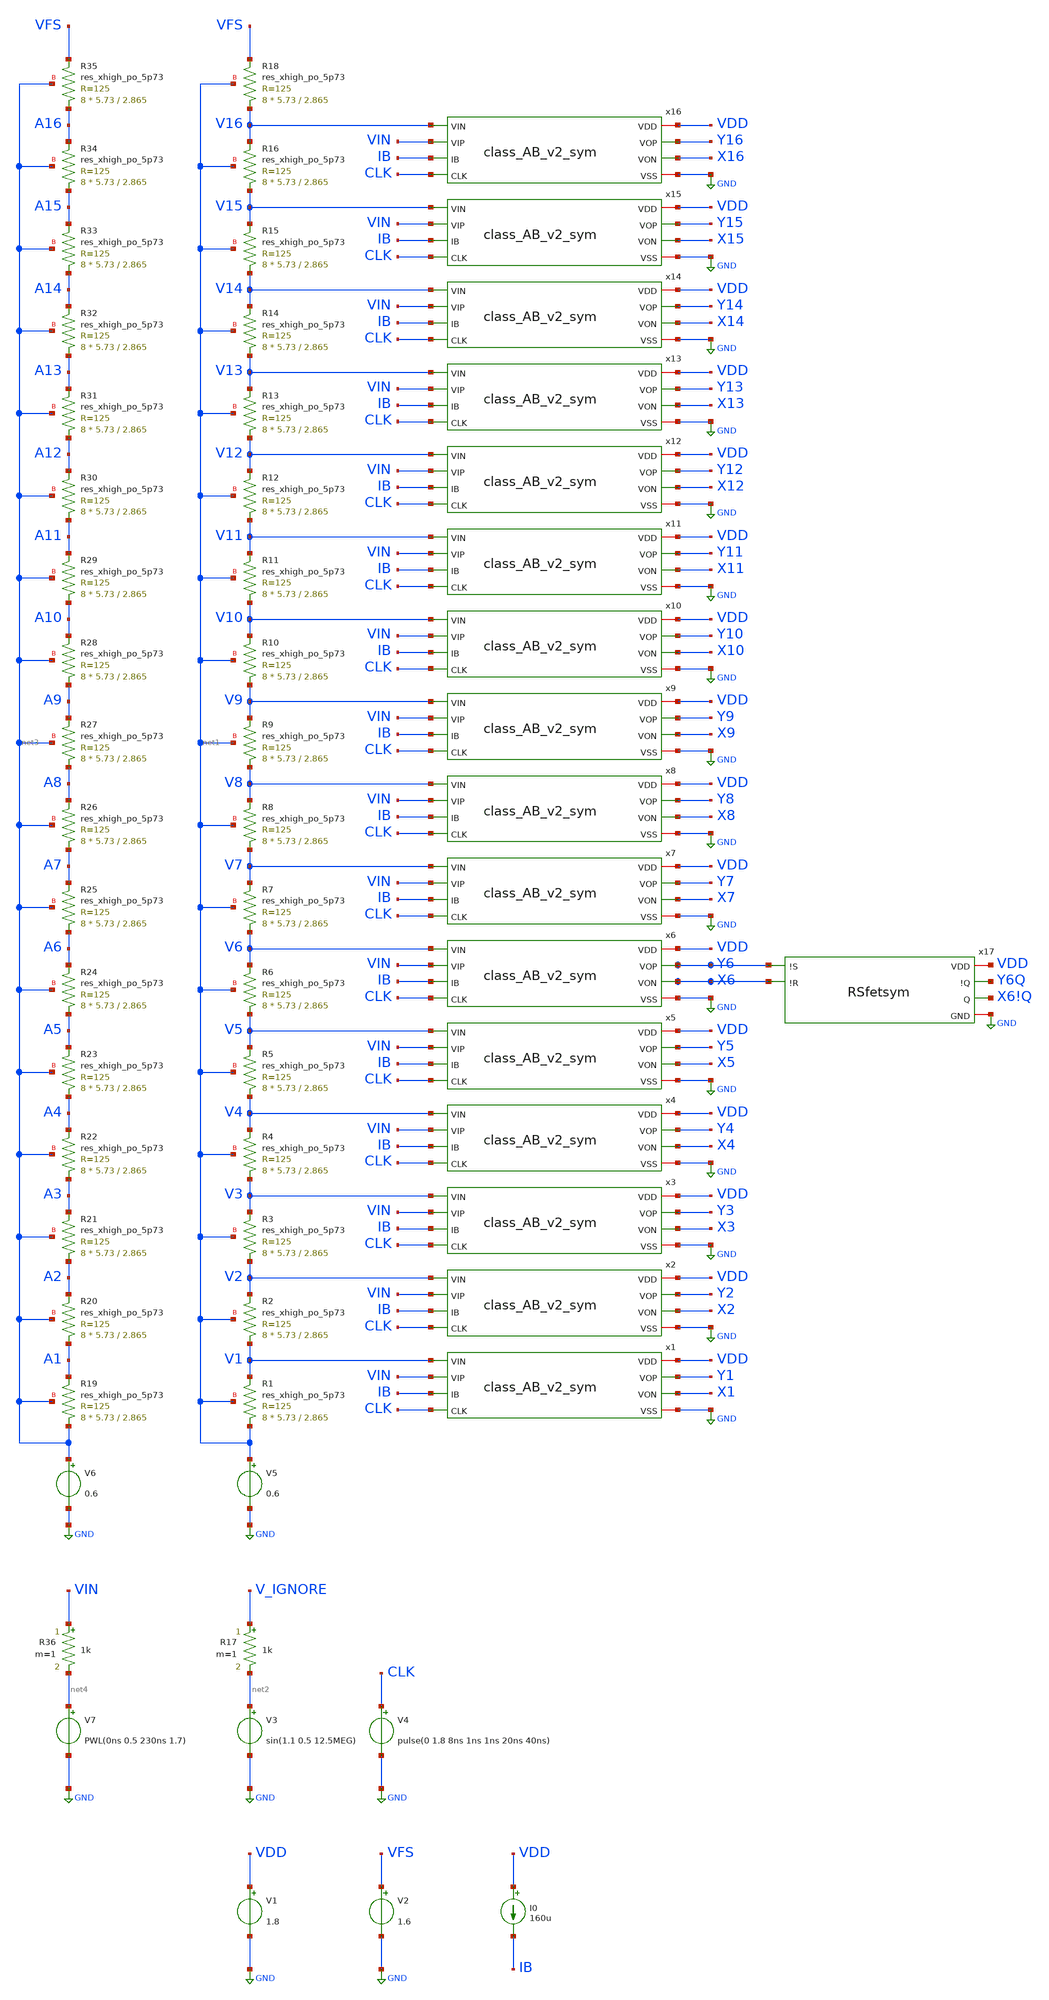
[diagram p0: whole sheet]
** sch_path: testbench/flash_ADC_4b_v2.sch
.lib $::SKYWATER_MODELS/sky130.lib.spice tt
.include $::SKYWATER_STDCELLS/sky130_fd_sc_hd.spice

**.subckt flash_ADC_4b_v2
V3 net2 GND sin(1.1 0.5 12.5MEG)
V4 CLK GND pulse(0 1.8 8ns 1ns 1ns 20ns 40ns)
V1 VDD GND 1.8
V2 VFS GND 1.6
R17 V_IGNORE net2 1k m=1
I0 VDD IB 160u
V5 net1 GND 0.6
XR19 net3 A1 net3 sky130_fd_pr__res_xhigh_po_5p73 L=2.865 mult=8 m=8
V6 net3 GND 0.6
XR20 A1 A2 net3 sky130_fd_pr__res_xhigh_po_5p73 L=2.865 mult=8 m=8
XR21 A2 A3 net3 sky130_fd_pr__res_xhigh_po_5p73 L=2.865 mult=8 m=8
XR22 A3 A4 net3 sky130_fd_pr__res_xhigh_po_5p73 L=2.865 mult=8 m=8
XR23 A4 A5 net3 sky130_fd_pr__res_xhigh_po_5p73 L=2.865 mult=8 m=8
XR24 A5 A6 net3 sky130_fd_pr__res_xhigh_po_5p73 L=2.865 mult=8 m=8
XR25 A6 A7 net3 sky130_fd_pr__res_xhigh_po_5p73 L=2.865 mult=8 m=8
XR26 A7 A8 net3 sky130_fd_pr__res_xhigh_po_5p73 L=2.865 mult=8 m=8
XR27 A8 A9 net3 sky130_fd_pr__res_xhigh_po_5p73 L=2.865 mult=8 m=8
XR28 A9 A10 net3 sky130_fd_pr__res_xhigh_po_5p73 L=2.865 mult=8 m=8
XR29 A10 A11 net3 sky130_fd_pr__res_xhigh_po_5p73 L=2.865 mult=8 m=8
XR30 A11 A12 net3 sky130_fd_pr__res_xhigh_po_5p73 L=2.865 mult=8 m=8
XR31 A12 A13 net3 sky130_fd_pr__res_xhigh_po_5p73 L=2.865 mult=8 m=8
XR32 A13 A14 net3 sky130_fd_pr__res_xhigh_po_5p73 L=2.865 mult=8 m=8
XR33 A14 A15 net3 sky130_fd_pr__res_xhigh_po_5p73 L=2.865 mult=8 m=8
XR34 A15 A16 net3 sky130_fd_pr__res_xhigh_po_5p73 L=2.865 mult=8 m=8
XR35 A16 VFS net3 sky130_fd_pr__res_xhigh_po_5p73 L=2.865 mult=8 m=8
XR1 net1 V1 net1 sky130_fd_pr__res_xhigh_po_5p73 L=2.865 mult=8 m=8
XR2 V1 V2 net1 sky130_fd_pr__res_xhigh_po_5p73 L=2.865 mult=8 m=8
XR3 V2 V3 net1 sky130_fd_pr__res_xhigh_po_5p73 L=2.865 mult=8 m=8
XR4 V3 V4 net1 sky130_fd_pr__res_xhigh_po_5p73 L=2.865 mult=8 m=8
XR5 V4 V5 net1 sky130_fd_pr__res_xhigh_po_5p73 L=2.865 mult=8 m=8
XR6 V5 V6 net1 sky130_fd_pr__res_xhigh_po_5p73 L=2.865 mult=8 m=8
XR7 V6 V7 net1 sky130_fd_pr__res_xhigh_po_5p73 L=2.865 mult=8 m=8
XR8 V7 V8 net1 sky130_fd_pr__res_xhigh_po_5p73 L=2.865 mult=8 m=8
XR9 V8 V9 net1 sky130_fd_pr__res_xhigh_po_5p73 L=2.865 mult=8 m=8
XR10 V9 V10 net1 sky130_fd_pr__res_xhigh_po_5p73 L=2.865 mult=8 m=8
XR11 V10 V11 net1 sky130_fd_pr__res_xhigh_po_5p73 L=2.865 mult=8 m=8
XR12 V11 V12 net1 sky130_fd_pr__res_xhigh_po_5p73 L=2.865 mult=8 m=8
XR13 V12 V13 net1 sky130_fd_pr__res_xhigh_po_5p73 L=2.865 mult=8 m=8
XR14 V13 V14 net1 sky130_fd_pr__res_xhigh_po_5p73 L=2.865 mult=8 m=8
XR15 V14 V15 net1 sky130_fd_pr__res_xhigh_po_5p73 L=2.865 mult=8 m=8
XR16 V15 V16 net1 sky130_fd_pr__res_xhigh_po_5p73 L=2.865 mult=8 m=8
XR18 V16 VFS net1 sky130_fd_pr__res_xhigh_po_5p73 L=2.865 mult=8 m=8
V7 net4 GND PWL(0ns 0.5 230ns 1.7)
R36 VIN net4 1k m=1
x1 VDD Y1 X1 V1 VIN IB CLK GND class_AB_v2_sym
x2 VDD Y2 X2 V2 VIN IB CLK GND class_AB_v2_sym
x3 VDD Y3 X3 V3 VIN IB CLK GND class_AB_v2_sym
x4 VDD Y4 X4 V4 VIN IB CLK GND class_AB_v2_sym
x5 VDD Y5 X5 V5 VIN IB CLK GND class_AB_v2_sym
x6 VDD Y6 X6 V6 VIN IB CLK GND class_AB_v2_sym
x7 VDD Y7 X7 V7 VIN IB CLK GND class_AB_v2_sym
x8 VDD Y8 X8 V8 VIN IB CLK GND class_AB_v2_sym
x9 VDD Y9 X9 V9 VIN IB CLK GND class_AB_v2_sym
x10 VDD Y10 X10 V10 VIN IB CLK GND class_AB_v2_sym
x11 VDD Y11 X11 V11 VIN IB CLK GND class_AB_v2_sym
x12 VDD Y12 X12 V12 VIN IB CLK GND class_AB_v2_sym
x13 VDD Y13 X13 V13 VIN IB CLK GND class_AB_v2_sym
x14 VDD Y14 X14 V14 VIN IB CLK GND class_AB_v2_sym
x15 VDD Y15 X15 V15 VIN IB CLK GND class_AB_v2_sym
x16 VDD Y16 X16 V16 VIN IB CLK GND class_AB_v2_sym
x17 VDD Y6 X6 Y6Q X6!Q GND RSfetsym
**** begin user architecture code


.options savecurrents
.control

save all

tran 0.005n 240n
remzerovec
write flash_ADC_4b_v2.raw

.endc


**** end user architecture code
**.ends
.GLOBAL GND
.end
